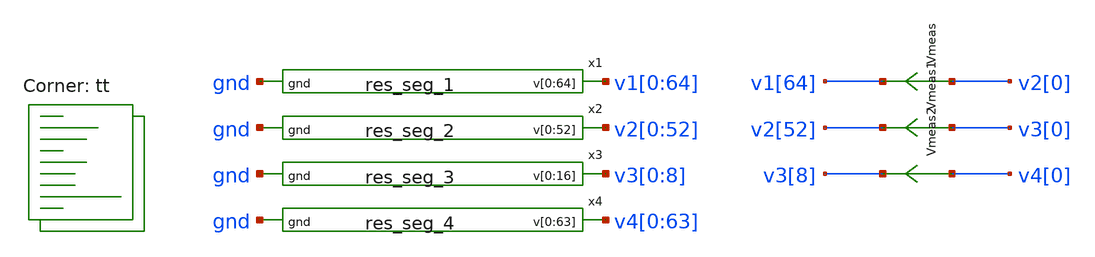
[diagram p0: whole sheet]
** sch_path: xschem/res_seg-tb.sch
**.subckt res_seg-tb
x1 v1[0] v1[1] v1[2] v1[3] v1[4] v1[5] v1[6] v1[7] v1[8] v1[9] v1[10] v1[11] v1[12] v1[13] v1[14]
+ v1[15] v1[16] v1[17] v1[18] v1[19] v1[20] v1[21] v1[22] v1[23] v1[24] v1[25] v1[26] v1[27] v1[28] v1[29]
+ v1[30] v1[31] v1[32] v1[33] v1[34] v1[35] v1[36] v1[37] v1[38] v1[39] v1[40] v1[41] v1[42] v1[43] v1[44]
+ v1[45] v1[46] v1[47] v1[48] v1[49] v1[50] v1[51] v1[52] v1[53] v1[54] v1[55] v1[56] v1[57] v1[58] v1[59]
+ v1[60] v1[61] v1[62] v1[63] v1[64] gnd res_seg_1
x2 v2[0] v2[1] v2[2] v2[3] v2[4] v2[5] v2[6] v2[7] v2[8] v2[9] v2[10] v2[11] v2[12] v2[13] v2[14]
+ v2[15] v2[16] v2[17] v2[18] v2[19] v2[20] v2[21] v2[22] v2[23] v2[24] v2[25] v2[26] v2[27] v2[28] v2[29]
+ v2[30] v2[31] v2[32] v2[33] v2[34] v2[35] v2[36] v2[37] v2[38] v2[39] v2[40] v2[41] v2[42] v2[43] v2[44]
+ v2[45] v2[46] v2[47] v2[48] v2[49] v2[50] v2[51] v2[52] gnd res_seg_2
x3 v3[0] v3[1] v3[2] v3[3] v3[4] v3[5] v3[6] v3[7] v3[8] v3[0] v3[1] v3[2] v3[3] v3[4] v3[5] v3[6]
+ v3[7] gnd res_seg_3
x4 v4[0] v4[1] v4[2] v4[3] v4[4] v4[5] v4[6] v4[7] v4[8] v4[9] v4[10] v4[11] v4[12] v4[13] v4[14]
+ v4[15] v4[16] v4[17] v4[18] v4[19] v4[20] v4[21] v4[22] v4[23] v4[24] v4[25] v4[26] v4[27] v4[28] v4[29]
+ v4[30] v4[31] v4[32] v4[33] v4[34] v4[35] v4[36] v4[37] v4[38] v4[39] v4[40] v4[41] v4[42] v4[43] v4[44]
+ v4[45] v4[46] v4[47] v4[48] v4[49] v4[50] v4[51] v4[52] v4[53] v4[54] v4[55] v4[56] v4[57] v4[58] v4[59]
+ v4[60] v4[61] v4[62] v4[63] gnd res_seg_4
Vmeas v2[0] v1[64] 0
.save i(vmeas)
Vmeas1 v3[0] v2[52] 0
.save i(vmeas1)
Vmeas2 v4[0] v3[8] 0
.save i(vmeas2)
**** begin user architecture code



  .param max_freq=500e3 period={1/max_freq} time_high={period/2}
  .param delay_vin1={time_high} delay_vin2={time_high*1.5}
  .param lval=100u

  .option wnflag=1
  .option safecurrents

  V4 v4[63] gnd dc 5
  v0 v1[0] gnd dc 0
  *Vin  in  gnd pulse(0 1.8 {delay_vin1} 1p 1p {time_high} {period})
  *Vinb inb gnd pulse(1.8 0 {delay_vin1} 1p 1p {time_high} {period})

  .control
     reset
     save all
     tran 1p 1n
     write res_seg-tb.raw
     set appendwrite

     *reset
     *save all
     *dc vref 0 1.8 0.1
     *write lvsf-tb.raw
*    quit 0
  .endc



.lib $::SKYWATER_MODELS/sky130.lib.spice tt
**** end user architecture code
**.ends

* expanding   symbol:  res_seg_1.sym # of pins=2
** sym_path: xschem/res_seg_1.sym
** sch_path: xschem/res_seg_1.sch
.subckt res_seg_1 v[0] v[1] v[2] v[3] v[4] v[5] v[6] v[7] v[8] v[9] v[10] v[11] v[12] v[13] v[14]
+ v[15] v[16] v[17] v[18] v[19] v[20] v[21] v[22] v[23] v[24] v[25] v[26] v[27] v[28] v[29] v[30] v[31]
+ v[32] v[33] v[34] v[35] v[36] v[37] v[38] v[39] v[40] v[41] v[42] v[43] v[44] v[45] v[46] v[47] v[48]
+ v[49] v[50] v[51] v[52] v[53] v[54] v[55] v[56] v[57] v[58] v[59] v[60] v[61] v[62] v[63] v[64] gnd
*.opin
*+ v[0],v[1],v[2],v[3],v[4],v[5],v[6],v[7],v[8],v[9],v[10],v[11],v[12],v[13],v[14],v[15],v[16],v[17],v[18],v[19],v[20],v[21],v[22],v[23],v[24],v[25],v[26],v[27],v[28],v[29],v[30],v[31],v[32],v[33],v[34],v[35],v[36],v[37],v[38],v[39],v[40],v[41],v[42],v[43],v[44],v[45],v[46],v[47],v[48],v[49],v[50],v[51],v[52],v[53],v[54],v[55],v[56],v[57],v[58],v[59],v[60],v[61],v[62],v[63],v[64]
*.ipin gnd
XR1 v[1] v[0] gnd sky130_fd_pr__res_xhigh_po_0p35 L=0.6495 mult=1 m=1
XR2 v[2] v[1] gnd sky130_fd_pr__res_xhigh_po_0p35 L=0.5897 mult=1 m=1
XR3 v[3] v[2] gnd sky130_fd_pr__res_xhigh_po_0p35 L=0.5469 mult=1 m=1
XR4 v[4] v[3] gnd sky130_fd_pr__res_xhigh_po_0p35 L=0.5042 mult=1 m=1
XR5 v[4] v[5] gnd sky130_fd_pr__res_xhigh_po_0p69 L=0.9266 mult=1 m=1
XR6 v[5] v[6] gnd sky130_fd_pr__res_xhigh_po_0p69 L=0.8592 mult=1 m=1
XR7 v[6] v[7] gnd sky130_fd_pr__res_xhigh_po_0p69 L=0.8255 mult=1 m=1
XR8 v[7] v[8] gnd sky130_fd_pr__res_xhigh_po_0p69 L=0.775 mult=1 m=1
XR9 v[8] v[9] gnd sky130_fd_pr__res_xhigh_po_0p69 L=0.7413 mult=1 m=1
XR10 v[9] v[10] gnd sky130_fd_pr__res_xhigh_po_0p69 L=0.7076 mult=1 m=1
XR11 v[10] v[11] gnd sky130_fd_pr__res_xhigh_po_0p69 L=0.6907 mult=1 m=1
XR12 v[11] v[12] gnd sky130_fd_pr__res_xhigh_po_0p69 L=0.6402 mult=1 m=1
XR13 v[12] v[13] gnd sky130_fd_pr__res_xhigh_po_0p69 L=0.6234 mult=1 m=1
XR14 v[13] v[14] gnd sky130_fd_pr__res_xhigh_po_0p69 L=0.6065 mult=1 m=1
XR15 v[14] v[15] gnd sky130_fd_pr__res_xhigh_po_0p69 L=0.5897 mult=1 m=1
XR16 v[15] v[16] gnd sky130_fd_pr__res_xhigh_po_0p69 L=0.556 mult=1 m=1
XR17 v[16] v[17] gnd sky130_fd_pr__res_xhigh_po_0p69 L=0.556 mult=1 m=1
XR18 v[17] v[18] gnd sky130_fd_pr__res_xhigh_po_0p69 L=0.5223 mult=1 m=1
XR19 v[18] v[19] gnd sky130_fd_pr__res_xhigh_po_0p69 L=0.5223 mult=1 m=1
XR20 v[19] v[20] gnd sky130_fd_pr__res_xhigh_po_1p41 L=0.9984 mult=1 m=1
XR21 v[20] v[21] gnd sky130_fd_pr__res_xhigh_po_1p41 L=0.9984 mult=1 m=1
XR22 v[21] v[22] gnd sky130_fd_pr__res_xhigh_po_1p41 L=0.9984 mult=1 m=1
XR23 v[22] v[23] gnd sky130_fd_pr__res_xhigh_po_1p41 L=0.9295 mult=1 m=1
XR24 v[23] v[24] gnd sky130_fd_pr__res_xhigh_po_1p41 L=0.9295 mult=1 m=1
XR25 v[24] v[25] gnd sky130_fd_pr__res_xhigh_po_1p41 L=0.9295 mult=1 m=1
XR26 v[25] v[26] gnd sky130_fd_pr__res_xhigh_po_1p41 L=0.8607 mult=1 m=1
XR27 v[26] v[27] gnd sky130_fd_pr__res_xhigh_po_1p41 L=0.8607 mult=1 m=1
XR28 v[27] v[28] gnd sky130_fd_pr__res_xhigh_po_1p41 L=0.8607 mult=1 m=1
XR29 v[28] v[29] gnd sky130_fd_pr__res_xhigh_po_1p41 L=0.8263 mult=1 m=1
XR30 v[29] v[30] gnd sky130_fd_pr__res_xhigh_po_1p41 L=0.8263 mult=1 m=1
XR31 v[30] v[31] gnd sky130_fd_pr__res_xhigh_po_1p41 L=0.7918 mult=1 m=1
XR32 v[31] v[32] gnd sky130_fd_pr__res_xhigh_po_1p41 L=0.7918 mult=1 m=1
XR33 v[32] v[33] gnd sky130_fd_pr__res_xhigh_po_1p41 L=0.7918 mult=1 m=1
XR34 v[33] v[34] gnd sky130_fd_pr__res_xhigh_po_1p41 L=0.7574 mult=1 m=1
XR35 v[34] v[35] gnd sky130_fd_pr__res_xhigh_po_1p41 L=0.723 mult=1 m=1
XR36 v[35] v[36] gnd sky130_fd_pr__res_xhigh_po_1p41 L=0.7574 mult=1 m=1
XR37 v[36] v[37] gnd sky130_fd_pr__res_xhigh_po_1p41 L=0.723 mult=1 m=1
XR38 v[37] v[38] gnd sky130_fd_pr__res_xhigh_po_1p41 L=0.6885 mult=1 m=1
XR39 v[38] v[39] gnd sky130_fd_pr__res_xhigh_po_1p41 L=0.723 mult=1 m=1
XR40 v[39] v[40] gnd sky130_fd_pr__res_xhigh_po_1p41 L=0.6885 mult=1 m=1
XR41 v[40] v[41] gnd sky130_fd_pr__res_xhigh_po_1p41 L=0.6885 mult=1 m=1
XR42 v[41] v[42] gnd sky130_fd_pr__res_xhigh_po_1p41 L=0.6541 mult=1 m=1
XR43 v[42] v[43] gnd sky130_fd_pr__res_xhigh_po_1p41 L=0.6541 mult=1 m=1
XR44 v[43] v[44] gnd sky130_fd_pr__res_xhigh_po_1p41 L=0.6541 mult=1 m=1
XR45 v[44] v[45] gnd sky130_fd_pr__res_xhigh_po_1p41 L=0.6541 mult=1 m=1
XR46 v[45] v[46] gnd sky130_fd_pr__res_xhigh_po_1p41 L=0.6197 mult=1 m=1
XR47 v[46] v[47] gnd sky130_fd_pr__res_xhigh_po_1p41 L=0.6541 mult=1 m=1
XR48 v[47] v[48] gnd sky130_fd_pr__res_xhigh_po_1p41 L=0.6197 mult=1 m=1
XR49 v[48] v[49] gnd sky130_fd_pr__res_xhigh_po_1p41 L=0.5853 mult=1 m=1
XR50 v[49] v[50] gnd sky130_fd_pr__res_xhigh_po_1p41 L=0.6197 mult=1 m=1
XR51 v[50] v[51] gnd sky130_fd_pr__res_xhigh_po_1p41 L=0.5853 mult=1 m=1
XR52 v[51] v[52] gnd sky130_fd_pr__res_xhigh_po_1p41 L=0.5853 mult=1 m=1
XR53 v[52] v[53] gnd sky130_fd_pr__res_xhigh_po_1p41 L=0.5853 mult=1 m=1
XR54 v[53] v[54] gnd sky130_fd_pr__res_xhigh_po_1p41 L=0.5853 mult=1 m=1
XR55 v[54] v[55] gnd sky130_fd_pr__res_xhigh_po_1p41 L=0.5853 mult=1 m=1
XR56 v[55] v[56] gnd sky130_fd_pr__res_xhigh_po_1p41 L=0.5508 mult=1 m=1
XR57 v[56] v[57] gnd sky130_fd_pr__res_xhigh_po_1p41 L=0.5508 mult=1 m=1
XR58 v[57] v[58] gnd sky130_fd_pr__res_xhigh_po_1p41 L=0.5508 mult=1 m=1
XR59 v[58] v[59] gnd sky130_fd_pr__res_xhigh_po_1p41 L=0.5508 mult=1 m=1
XR60 v[59] v[60] gnd sky130_fd_pr__res_xhigh_po_1p41 L=0.5508 mult=1 m=1
XR61 v[60] v[61] gnd sky130_fd_pr__res_xhigh_po_1p41 L=0.5508 mult=1 m=1
XR62 v[61] v[62] gnd sky130_fd_pr__res_xhigh_po_1p41 L=0.5164 mult=1 m=1
XR63 v[62] v[63] gnd sky130_fd_pr__res_xhigh_po_1p41 L=0.5164 mult=1 m=1
XR64 v[63] v[64] gnd sky130_fd_pr__res_xhigh_po_1p41 L=0.5508 mult=1 m=1
.ends


* expanding   symbol:  res_seg_2.sym # of pins=2
** sym_path: xschem/res_seg_2.sym
** sch_path: xschem/res_seg_2.sch
.subckt res_seg_2 v[0] v[1] v[2] v[3] v[4] v[5] v[6] v[7] v[8] v[9] v[10] v[11] v[12] v[13] v[14]
+ v[15] v[16] v[17] v[18] v[19] v[20] v[21] v[22] v[23] v[24] v[25] v[26] v[27] v[28] v[29] v[30] v[31]
+ v[32] v[33] v[34] v[35] v[36] v[37] v[38] v[39] v[40] v[41] v[42] v[43] v[44] v[45] v[46] v[47] v[48]
+ v[49] v[50] v[51] v[52] gnd
*.opin
*+ v[0],v[1],v[2],v[3],v[4],v[5],v[6],v[7],v[8],v[9],v[10],v[11],v[12],v[13],v[14],v[15],v[16],v[17],v[18],v[19],v[20],v[21],v[22],v[23],v[24],v[25],v[26],v[27],v[28],v[29],v[30],v[31],v[32],v[33],v[34],v[35],v[36],v[37],v[38],v[39],v[40],v[41],v[42],v[43],v[44],v[45],v[46],v[47],v[48],v[49],v[50],v[51],v[52]
*.ipin gnd
XR1 v[1] v[0] gnd sky130_fd_pr__res_xhigh_po_0p35 L=1.9228 mult=1 m=1
XR2 v[2] v[1] gnd sky130_fd_pr__res_xhigh_po_0p35 L=1.7092 mult=1 m=1
XR3 v[3] v[2] gnd sky130_fd_pr__res_xhigh_po_0p35 L=1.5468 mult=1 m=1
XR4 v[4] v[3] gnd sky130_fd_pr__res_xhigh_po_0p35 L=1.4357 mult=1 m=1
XR5 v[5] v[4] gnd sky130_fd_pr__res_xhigh_po_0p35 L=1.3246 mult=1 m=1
XR6 v[6] v[5] gnd sky130_fd_pr__res_xhigh_po_0p35 L=1.2562 mult=1 m=1
XR7 v[7] v[6] gnd sky130_fd_pr__res_xhigh_po_0p35 L=1.1879 mult=1 m=1
XR8 v[8] v[7] gnd sky130_fd_pr__res_xhigh_po_0p35 L=1.128 mult=1 m=1
XR9 v[9] v[8] gnd sky130_fd_pr__res_xhigh_po_0p35 L=1.0853 mult=1 m=1
XR10 v[10] v[9] gnd sky130_fd_pr__res_xhigh_po_0p35 L=1.0511 mult=1 m=1
XR11 v[11] v[10] gnd sky130_fd_pr__res_xhigh_po_0p35 L=1.0084 mult=1 m=1
XR12 v[12] v[11] gnd sky130_fd_pr__res_xhigh_po_0p35 L=0.9828 mult=1 m=1
XR13 v[13] v[12] gnd sky130_fd_pr__res_xhigh_po_0p35 L=0.9571 mult=1 m=1
XR14 v[14] v[13] gnd sky130_fd_pr__res_xhigh_po_0p35 L=0.9315 mult=1 m=1
XR15 v[15] v[14] gnd sky130_fd_pr__res_xhigh_po_0p35 L=0.9059 mult=1 m=1
XR16 v[16] v[15] gnd sky130_fd_pr__res_xhigh_po_0p35 L=0.8973 mult=1 m=1
XR17 v[17] v[16] gnd sky130_fd_pr__res_xhigh_po_0p35 L=0.8802 mult=1 m=1
XR18 v[18] v[17] gnd sky130_fd_pr__res_xhigh_po_0p35 L=0.8631 mult=1 m=1
XR19 v[19] v[18] gnd sky130_fd_pr__res_xhigh_po_0p35 L=0.8546 mult=1 m=1
XR20 v[20] v[19] gnd sky130_fd_pr__res_xhigh_po_0p35 L=0.8375 mult=1 m=1
XR21 v[21] v[20] gnd sky130_fd_pr__res_xhigh_po_0p35 L=0.8375 mult=1 m=1
XR22 v[22] v[21] gnd sky130_fd_pr__res_xhigh_po_0p35 L=0.8289 mult=1 m=1
XR23 v[23] v[22] gnd sky130_fd_pr__res_xhigh_po_0p35 L=0.8204 mult=1 m=1
XR24 v[24] v[23] gnd sky130_fd_pr__res_xhigh_po_0p35 L=0.8118 mult=1 m=1
XR25 v[25] v[24] gnd sky130_fd_pr__res_xhigh_po_0p35 L=0.8118 mult=1 m=1
XR27 v[27] v[26] gnd sky130_fd_pr__res_xhigh_po_0p35 L=0.8033 mult=1 m=1
XR33 v[33] v[32] gnd sky130_fd_pr__res_xhigh_po_0p35 L=0.8204 mult=1 m=1
XR35 v[35] v[34] gnd sky130_fd_pr__res_xhigh_po_0p35 L=0.8289 mult=1 m=1
XR36 v[36] v[35] gnd sky130_fd_pr__res_xhigh_po_0p35 L=0.8460 mult=1 m=1
XR38 v[38] v[37] gnd sky130_fd_pr__res_xhigh_po_0p35 L=0.8631 mult=1 m=1
XR39 v[39] v[38] gnd sky130_fd_pr__res_xhigh_po_0p35 L=0.8717 mult=1 m=1
XR40 v[40] v[39] gnd sky130_fd_pr__res_xhigh_po_0p35 L=0.8802 mult=1 m=1
XR41 v[41] v[40] gnd sky130_fd_pr__res_xhigh_po_0p35 L=0.9059 mult=1 m=1
XR42 v[42] v[41] gnd sky130_fd_pr__res_xhigh_po_0p35 L=0.9144 mult=1 m=1
XR43 v[43] v[42] gnd sky130_fd_pr__res_xhigh_po_0p35 L=0.94 mult=1 m=1
XR44 v[44] v[43] gnd sky130_fd_pr__res_xhigh_po_0p35 L=0.9657 mult=1 m=1
XR45 v[45] v[44] gnd sky130_fd_pr__res_xhigh_po_0p35 L=0.9913 mult=1 m=1
XR46 v[46] v[45] gnd sky130_fd_pr__res_xhigh_po_0p35 L=1.0169 mult=1 m=1
XR47 v[47] v[46] gnd sky130_fd_pr__res_xhigh_po_0p35 L=1.0511 mult=1 m=1
XR48 v[48] v[47] gnd sky130_fd_pr__res_xhigh_po_0p35 L=1.0853 mult=1 m=1
XR49 v[49] v[48] gnd sky130_fd_pr__res_xhigh_po_0p35 L=1.1366 mult=1 m=1
XR50 v[50] v[49] gnd sky130_fd_pr__res_xhigh_po_0p35 L=1.1879 mult=1 m=1
XR51 v[51] v[50] gnd sky130_fd_pr__res_xhigh_po_0p35 L=1.2477 mult=1 m=1
XR52 v[52] v[51] gnd sky130_fd_pr__res_xhigh_po_0p35 L=1.316 mult=1 m=1
XR26 v[26] v[25] gnd sky130_fd_pr__res_xhigh_po_0p35 L=0.8118 mult=1 m=1
XR28 v[28] v[27] gnd sky130_fd_pr__res_xhigh_po_0p35 L=0.8118 mult=1 m=1
XR29 v[29] v[28] gnd sky130_fd_pr__res_xhigh_po_0p35 L=0.8033 mult=1 m=1
XR30 v[30] v[29] gnd sky130_fd_pr__res_xhigh_po_0p35 L=0.8118 mult=1 m=1
XR31 v[31] v[30] gnd sky130_fd_pr__res_xhigh_po_0p35 L=0.8118 mult=1 m=1
XR32 v[32] v[31] gnd sky130_fd_pr__res_xhigh_po_0p35 L=0.8118 mult=1 m=1
XR34 v[34] v[33] gnd sky130_fd_pr__res_xhigh_po_0p35 L=0.8204 mult=1 m=1
XR37 v[37] v[36] gnd sky130_fd_pr__res_xhigh_po_0p35 L=0.8460 mult=1 m=1
.ends


* expanding   symbol:  res_seg_3.sym # of pins=2
** sym_path: xschem/res_seg_3.sym
** sch_path: xschem/res_seg_3.sch
.subckt res_seg_3 v[0] v[1] v[2] v[3] v[4] v[5] v[6] v[7] v[8] v[9] v[10] v[11] v[12] v[13] v[14]
+ v[15] v[16] gnd
*.opin v[0],v[1],v[2],v[3],v[4],v[5],v[6],v[7],v[8],v[9],v[10],v[11],v[12],v[13],v[14],v[15],v[16]
*.ipin gnd
XR1 v[0] v[1] gnd sky130_fd_pr__res_xhigh_po_0p35 L=0.5555 mult=1 m=1
XR2 v[1] v[2] gnd sky130_fd_pr__res_xhigh_po_0p35 L=0.5726 mult=1 m=1
XR3 v[2] v[3] gnd sky130_fd_pr__res_xhigh_po_0p35 L=0.5811 mult=1 m=1
XR4 v[3] v[4] gnd sky130_fd_pr__res_xhigh_po_0p35 L=0.5897 mult=1 m=1
XR5 v[4] v[5] gnd sky130_fd_pr__res_xhigh_po_0p35 L=0.6153 mult=1 m=1
XR6 v[5] v[6] gnd sky130_fd_pr__res_xhigh_po_0p35 L=0.6238 mult=1 m=1
XR7 v[6] v[7] gnd sky130_fd_pr__res_xhigh_po_0p35 L=0.6409 mult=1 m=1
XR8 v[7] v[8] gnd sky130_fd_pr__res_xhigh_po_0p35 L=0.6666 mult=1 m=1
XR9 v[8] v[9] gnd sky130_fd_pr__res_xhigh_po_0p35 L=0.6837 mult=1 m=1
XR10 v[9] v[10] gnd sky130_fd_pr__res_xhigh_po_0p35 L=0.7093 mult=1 m=1
XR11 v[10] v[11] gnd sky130_fd_pr__res_xhigh_po_0p35 L=0.7264 mult=1 m=1
XR12 v[11] v[12] gnd sky130_fd_pr__res_xhigh_po_0p35 L=0.7691 mult=1 m=1
XR13 v[12] v[13] gnd sky130_fd_pr__res_xhigh_po_0p35 L=0.7948 mult=1 m=1
XR14 v[13] v[14] gnd sky130_fd_pr__res_xhigh_po_0p35 L=0.8375 mult=1 m=1
XR15 v[14] v[15] gnd sky130_fd_pr__res_xhigh_po_0p35 L=0.8802 mult=1 m=1
XR16 v[15] v[16] gnd sky130_fd_pr__res_xhigh_po_0p35 L=0.9315 mult=1 m=1
.ends


* expanding   symbol:  res_seg_4.sym # of pins=2
** sym_path: xschem/res_seg_4.sym
** sch_path: xschem/res_seg_4.sch
.subckt res_seg_4 v[0] v[1] v[2] v[3] v[4] v[5] v[6] v[7] v[8] v[9] v[10] v[11] v[12] v[13] v[14]
+ v[15] v[16] v[17] v[18] v[19] v[20] v[21] v[22] v[23] v[24] v[25] v[26] v[27] v[28] v[29] v[30] v[31]
+ v[32] v[33] v[34] v[35] v[36] v[37] v[38] v[39] v[40] v[41] v[42] v[43] v[44] v[45] v[46] v[47] v[48]
+ v[49] v[50] v[51] v[52] v[53] v[54] v[55] v[56] v[57] v[58] v[59] v[60] v[61] v[62] v[63] gnd
*.opin
*+ v[0],v[1],v[2],v[3],v[4],v[5],v[6],v[7],v[8],v[9],v[10],v[11],v[12],v[13],v[14],v[15],v[16],v[17],v[18],v[19],v[20],v[21],v[22],v[23],v[24],v[25],v[26],v[27],v[28],v[29],v[30],v[31],v[32],v[33],v[34],v[35],v[36],v[37],v[38],v[39],v[40],v[41],v[42],v[43],v[44],v[45],v[46],v[47],v[48],v[49],v[50],v[51],v[52],v[53],v[54],v[55],v[56],v[57],v[58],v[59],v[60],v[61],v[62],v[63]
*.ipin gnd
XR1 v[0] v[1] gnd sky130_fd_pr__res_xhigh_po_2p85 L=0.9742 mult=1 m=1
XR2 v[1] v[2] gnd sky130_fd_pr__res_xhigh_po_1p41 L=0.5164 mult=1 m=1
XR3 v[2] v[3] gnd sky130_fd_pr__res_xhigh_po_1p41 L=0.5164 mult=1 m=1
XR4 v[3] v[4] gnd sky130_fd_pr__res_xhigh_po_2p85 L=0.9742 mult=1 m=1
XR5 v[4] v[5] gnd sky130_fd_pr__res_xhigh_po_1p41 L=0.5164 mult=1 m=1
XR6 v[5] v[6] gnd sky130_fd_pr__res_xhigh_po_1p41 L=0.5164 mult=1 m=1
XR7 v[6] v[7] gnd sky130_fd_pr__res_xhigh_po_1p41 L=0.5508 mult=1 m=1
XR8 v[7] v[8] gnd sky130_fd_pr__res_xhigh_po_1p41 L=0.5164 mult=1 m=1
XR9 v[8] v[9] gnd sky130_fd_pr__res_xhigh_po_1p41 L=0.5508 mult=1 m=1
XR10 v[9] v[10] gnd sky130_fd_pr__res_xhigh_po_1p41 L=0.5164 mult=1 m=1
XR11 v[10] v[11] gnd sky130_fd_pr__res_xhigh_po_1p41 L=0.5508 mult=1 m=1
XR12 v[11] v[12] gnd sky130_fd_pr__res_xhigh_po_1p41 L=0.5508 mult=1 m=1
XR13 v[12] v[13] gnd sky130_fd_pr__res_xhigh_po_1p41 L=0.5508 mult=1 m=1
XR14 v[13] v[14] gnd sky130_fd_pr__res_xhigh_po_1p41 L=0.5853 mult=1 m=1
XR15 v[14] v[15] gnd sky130_fd_pr__res_xhigh_po_1p41 L=0.5508 mult=1 m=1
XR16 v[15] v[16] gnd sky130_fd_pr__res_xhigh_po_1p41 L=0.5853 mult=1 m=1
XR17 v[16] v[17] gnd sky130_fd_pr__res_xhigh_po_1p41 L=0.5853 mult=1 m=1
XR18 v[17] v[18] gnd sky130_fd_pr__res_xhigh_po_1p41 L=0.5853 mult=1 m=1
XR19 v[18] v[19] gnd sky130_fd_pr__res_xhigh_po_1p41 L=0.5853 mult=1 m=1
XR20 v[19] v[20] gnd sky130_fd_pr__res_xhigh_po_1p41 L=0.6197 mult=1 m=1
XR21 v[20] v[21] gnd sky130_fd_pr__res_xhigh_po_1p41 L=0.5853 mult=1 m=1
XR22 v[21] v[22] gnd sky130_fd_pr__res_xhigh_po_1p41 L=0.6197 mult=1 m=1
XR23 v[22] v[23] gnd sky130_fd_pr__res_xhigh_po_1p41 L=0.6197 mult=1 m=1
XR24 v[23] v[24] gnd sky130_fd_pr__res_xhigh_po_1p41 L=0.6541 mult=1 m=1
XR25 v[24] v[25] gnd sky130_fd_pr__res_xhigh_po_1p41 L=0.6197 mult=1 m=1
XR26 v[25] v[26] gnd sky130_fd_pr__res_xhigh_po_1p41 L=0.6541 mult=1 m=1
XR27 v[26] v[27] gnd sky130_fd_pr__res_xhigh_po_1p41 L=0.6541 mult=1 m=1
XR28 v[27] v[28] gnd sky130_fd_pr__res_xhigh_po_1p41 L=0.6885 mult=1 m=1
XR29 v[28] v[29] gnd sky130_fd_pr__res_xhigh_po_1p41 L=0.6885 mult=1 m=1
XR30 v[29] v[30] gnd sky130_fd_pr__res_xhigh_po_1p41 L=0.6885 mult=1 m=1
XR31 v[30] v[31] gnd sky130_fd_pr__res_xhigh_po_1p41 L=0.6885 mult=1 m=1
XR32 v[31] v[32] gnd sky130_fd_pr__res_xhigh_po_1p41 L=0.723 mult=1 m=1
XR33 v[32] v[33] gnd sky130_fd_pr__res_xhigh_po_1p41 L=0.723 mult=1 m=1
XR34 v[33] v[34] gnd sky130_fd_pr__res_xhigh_po_1p41 L=0.723 mult=1 m=1
XR35 v[34] v[35] gnd sky130_fd_pr__res_xhigh_po_1p41 L=0.7574 mult=1 m=1
XR36 v[35] v[36] gnd sky130_fd_pr__res_xhigh_po_1p41 L=0.7574 mult=1 m=1
XR37 v[36] v[37] gnd sky130_fd_pr__res_xhigh_po_1p41 L=0.7574 mult=1 m=1
XR38 v[37] v[38] gnd sky130_fd_pr__res_xhigh_po_1p41 L=0.7918 mult=1 m=1
XR39 v[38] v[39] gnd sky130_fd_pr__res_xhigh_po_1p41 L=0.8263 mult=1 m=1
XR40 v[39] v[40] gnd sky130_fd_pr__res_xhigh_po_1p41 L=0.8263 mult=1 m=1
XR41 v[40] v[41] gnd sky130_fd_pr__res_xhigh_po_1p41 L=0.8263 mult=1 m=1
XR42 v[41] v[42] gnd sky130_fd_pr__res_xhigh_po_1p41 L=0.8607 mult=1 m=1
XR43 v[42] v[43] gnd sky130_fd_pr__res_xhigh_po_1p41 L=0.8951 mult=1 m=1
XR44 v[43] v[44] gnd sky130_fd_pr__res_xhigh_po_1p41 L=0.8951 mult=1 m=1
XR45 v[44] v[45] gnd sky130_fd_pr__res_xhigh_po_1p41 L=0.9295 mult=1 m=1
XR46 v[45] v[46] gnd sky130_fd_pr__res_xhigh_po_1p41 L=0.964 mult=1 m=1
XR47 v[46] v[47] gnd sky130_fd_pr__res_xhigh_po_1p41 L=0.964 mult=1 m=1
XR48 v[47] v[48] gnd sky130_fd_pr__res_xhigh_po_1p41 L=0.9984 mult=1 m=1
XR49 v[48] v[49] gnd sky130_fd_pr__res_xhigh_po_0p69 L=0.5223 mult=1 m=1
XR50 v[49] v[50] gnd sky130_fd_pr__res_xhigh_po_0p69 L=0.5223 mult=1 m=1
XR51 v[50] v[51] gnd sky130_fd_pr__res_xhigh_po_0p69 L=0.5391 mult=1 m=1
XR52 v[51] v[52] gnd sky130_fd_pr__res_xhigh_po_0p69 L=0.556 mult=1 m=1
XR53 v[52] v[53] gnd sky130_fd_pr__res_xhigh_po_0p69 L=0.5897 mult=1 m=1
XR54 v[53] v[54] gnd sky130_fd_pr__res_xhigh_po_0p69 L=0.6234 mult=1 m=1
XR55 v[54] v[55] gnd sky130_fd_pr__res_xhigh_po_0p69 L=0.6402 mult=1 m=1
XR56 v[55] v[56] gnd sky130_fd_pr__res_xhigh_po_0p69 L=0.6739 mult=1 m=1
XR57 v[56] v[57] gnd sky130_fd_pr__res_xhigh_po_0p69 L=0.7076 mult=1 m=1
XR58 v[57] v[58] gnd sky130_fd_pr__res_xhigh_po_0p69 L=0.775 mult=1 m=1
XR59 v[58] v[59] gnd sky130_fd_pr__res_xhigh_po_0p69 L=0.8087 mult=1 m=1
XR60 v[59] v[60] gnd sky130_fd_pr__res_xhigh_po_0p69 L=0.8929 mult=1 m=1
XR61 v[60] v[61] gnd sky130_fd_pr__res_xhigh_po_0p69 L=0.9603 mult=1 m=1
XR62 v[61] v[62] gnd sky130_fd_pr__res_xhigh_po_0p35 L=0.5555 mult=1 m=1
XR63 v[62] v[63] gnd sky130_fd_pr__res_xhigh_po_0p35 L=0.6409 mult=1 m=1
.ends

.end
